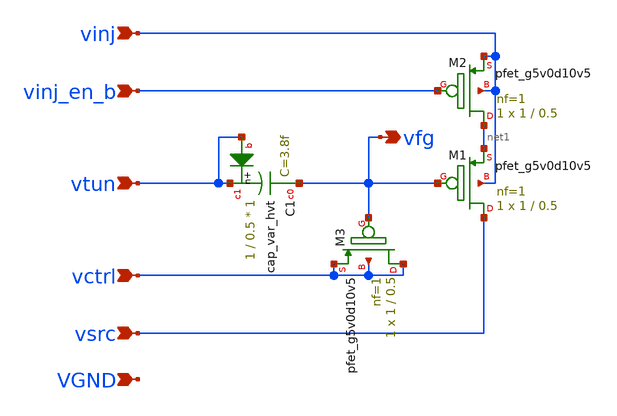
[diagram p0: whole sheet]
** sch_path: xschem/fgcell.sch
**.subckt fgcell vinj vinj_en_b vtun vctrl vsrc VGND vfg
*.ipin vinj
*.ipin vinj_en_b
*.ipin vtun
*.ipin vctrl
*.ipin vsrc
*.ipin VGND
*.opin vfg
XM1 vsrc vfg net1 vinj sky130_fd_pr__pfet_g5v0d10v5 L=0.5 W=1 nf=1 ad='int((nf+1)/2) * W/nf * 0.29' as='int((nf+2)/2) * W/nf * 0.29'
+ pd='2*int((nf+1)/2) * (W/nf + 0.29)' ps='2*int((nf+2)/2) * (W/nf + 0.29)' nrd='0.29 / W' nrs='0.29 / W'
+ sa=0 sb=0 sd=0 mult=1 m=1
XM2 net1 vinj_en_b vinj vinj sky130_fd_pr__pfet_g5v0d10v5 L=0.5 W=1 nf=1 ad='int((nf+1)/2) * W/nf * 0.29'
+ as='int((nf+2)/2) * W/nf * 0.29' pd='2*int((nf+1)/2) * (W/nf + 0.29)' ps='2*int((nf+2)/2) * (W/nf + 0.29)'
+ nrd='0.29 / W' nrs='0.29 / W' sa=0 sb=0 sd=0 mult=1 m=1
XC1 vfg vtun vtun sky130_fd_pr__cap_var_hvt W=1 L=0.5 VM=1 m=1
XM3 vctrl vfg vctrl vctrl sky130_fd_pr__pfet_g5v0d10v5 L=0.5 W=1 nf=1 ad='int((nf+1)/2) * W/nf * 0.29'
+ as='int((nf+2)/2) * W/nf * 0.29' pd='2*int((nf+1)/2) * (W/nf + 0.29)' ps='2*int((nf+2)/2) * (W/nf + 0.29)'
+ nrd='0.29 / W' nrs='0.29 / W' sa=0 sb=0 sd=0 mult=1 m=1
**.ends
.end
